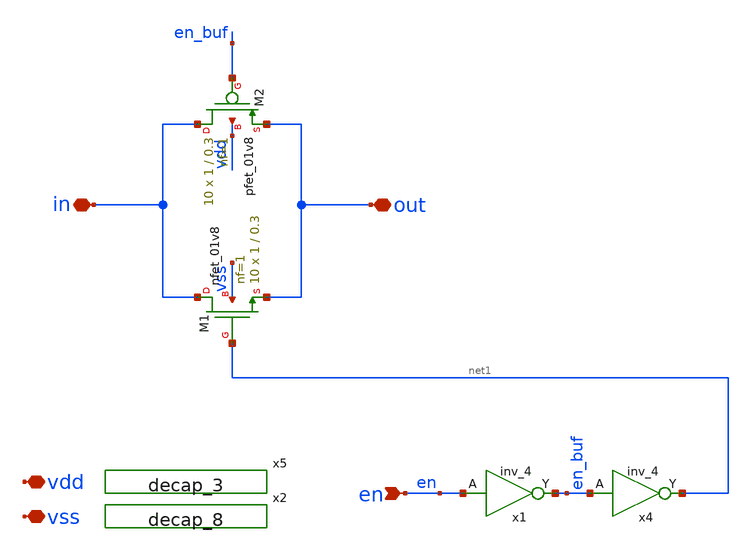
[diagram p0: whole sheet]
** sch_path: xschem/sar/sw/sw_top.sch
**.subckt sw_top out en vss vdd in
*.iopin out
*.ipin en
*.iopin vss
*.iopin vdd
*.iopin in
x2 vss vss vdd vdd sky130_fd_sc_hd__decap_8
x4 en_buf vss vss vdd vdd net1 sky130_fd_sc_hd__inv_4
x5 vss vss vdd vdd sky130_fd_sc_hd__decap_3
XM1 in net1 out vss sky130_fd_pr__nfet_01v8 L=0.3 W=1 nf=1 ad='int((nf+1)/2) * W/nf * 0.29' as='int((nf+2)/2) * W/nf * 0.29'
+ pd='2*int((nf+1)/2) * (W/nf + 0.29)' ps='2*int((nf+2)/2) * (W/nf + 0.29)' nrd='0.29 / W' nrs='0.29 / W'
+ sa=0 sb=0 sd=0 mult=10 m=10
XM2 in en_buf out vdd sky130_fd_pr__pfet_01v8 L=0.3 W=1 nf=1 ad='int((nf+1)/2) * W/nf * 0.29' as='int((nf+2)/2) * W/nf * 0.29'
+ pd='2*int((nf+1)/2) * (W/nf + 0.29)' ps='2*int((nf+2)/2) * (W/nf + 0.29)' nrd='0.29 / W' nrs='0.29 / W'
+ sa=0 sb=0 sd=0 mult=10 m=10
x1 en vss vss vdd vdd en_buf sky130_fd_sc_hd__inv_4
**.ends
.end
